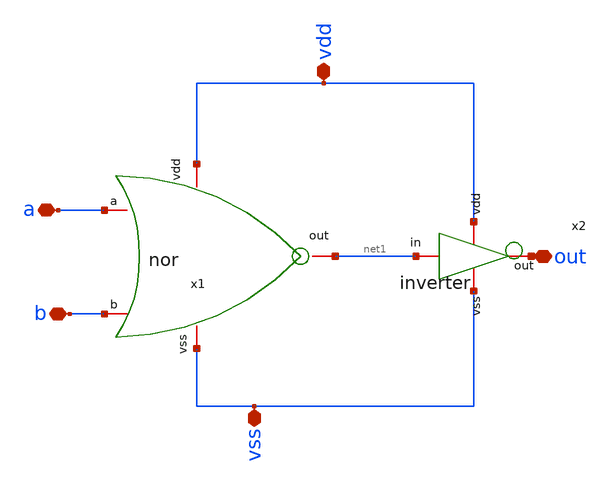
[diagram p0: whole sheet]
** sch_path: design/blocks/orgate/schematic/orgate.sch
**.subckt orgate a b vss vdd out
*.iopin a
*.iopin b
*.iopin vss
*.iopin vdd
*.iopin out
x2 vdd out net1 vss inverter
x1 vdd a b net1 vss nor
**.ends

* expanding   symbol:  blocks/inverter/schematic/inverter.sym # of pins=4
** sym_path: design/blocks/inverter/schematic/inverter.sym
** sch_path: design/blocks/inverter/schematic/inverter.sch
.subckt inverter vdd out in vss
*.iopin vdd
*.iopin out
*.iopin vss
*.iopin in
XM1 out in vss vss sg13_lv_nmos w=0.75u l=0.15u ng=1 m=1 mm_ok=1
XM2 out in vdd vdd sg13_lv_pmos w=1.5u l=0.15u ng=1 m=1 mm_ok=1
.ends


* expanding   symbol:  blocks/norgate/schematic/nor.sym # of pins=5
** sym_path: design/blocks/norgate/schematic/nor.sym
** sch_path: design/blocks/norgate/schematic/nor.sch
.subckt nor vdd a b out vss
*.iopin vdd
*.iopin a
*.iopin vss
*.iopin out
*.iopin b
XM1 net1 a vdd vdd sg13_lv_pmos w=3.0u l=0.15u ng=1 m=1 mm_ok=1
XM2 out b vss vss sg13_lv_nmos w=0.75u l=0.15u ng=1 m=1 mm_ok=1
XM3 out a vss vss sg13_lv_nmos w=0.75u l=0.15u ng=1 m=1 mm_ok=1
XM4 out b net1 vdd sg13_lv_pmos w=3.0u l=0.15u ng=1 m=1 mm_ok=1
.ends

.end
